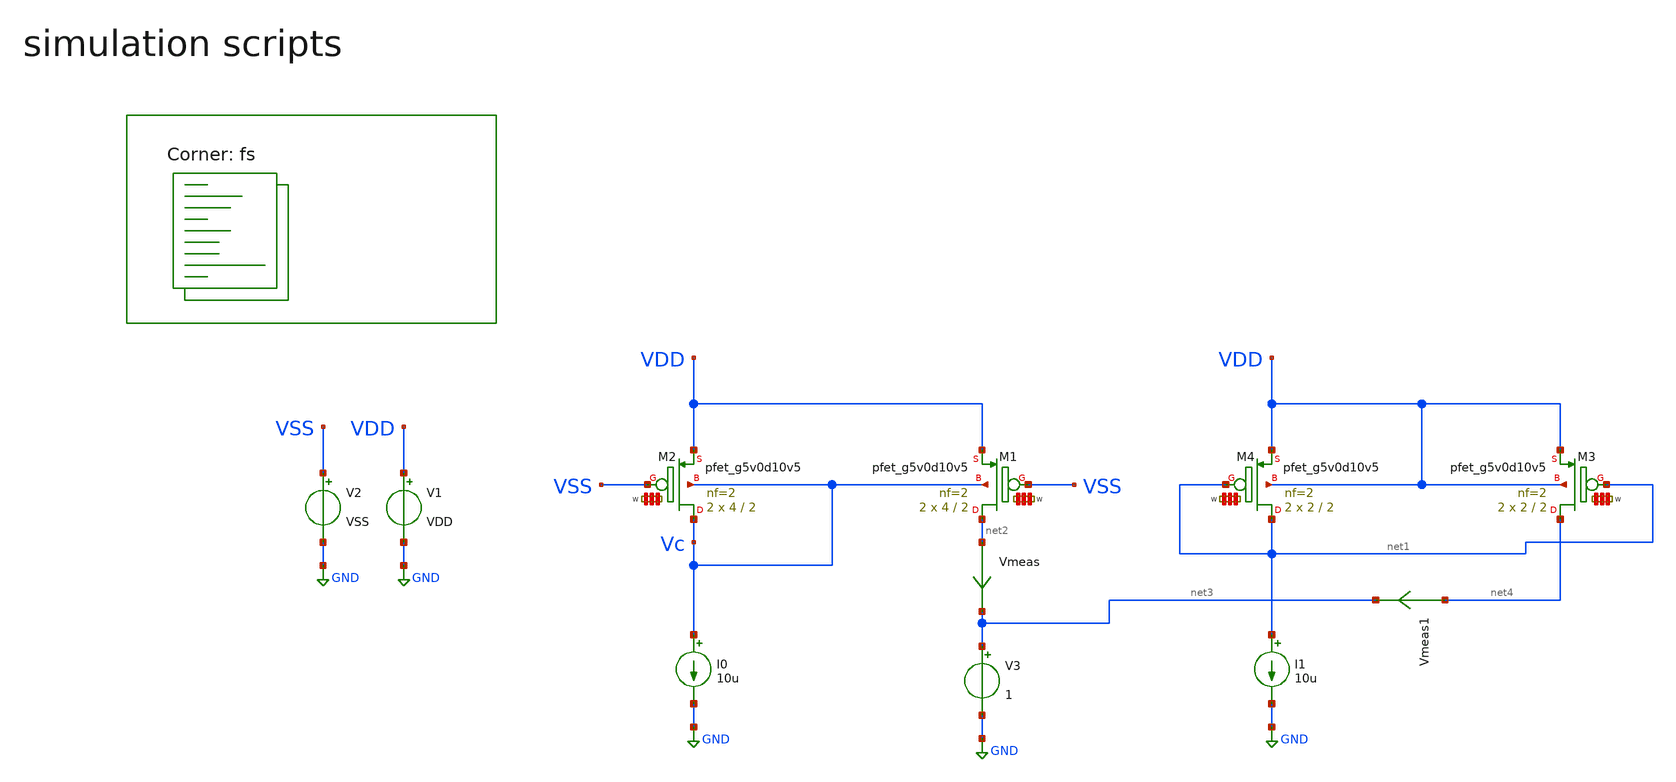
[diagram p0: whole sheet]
** sch_path: Learning/curr_amplifiers/bulk_curr_mir/tb.sch
**.subckt tb
V1 VDD GND VDD
V2 VSS GND VSS
V3 net3 GND 1
I0 Vc GND 10u
XM1 net2 VSS VDD Vc sky130_fd_pr__pfet_g5v0d10v5 L=2 W='4 * 2 ' nf=2 ad='int((2 + 1)/2) * 4 * 0.29' as='int((2 + 2)/2) * 4 * 0.29'
+ pd='2*int((2 + 1)/2) * (4 + 0.29)' ps='2*int((2 + 2)/2) * (4 + 0.29)' nrd='0.29 / 4 / 2 ' nrs='0.29 / 4 / 2 '
+ sa=0 sb=0 sd=0 mult=2 m=2
XM2 Vc VSS VDD Vc sky130_fd_pr__pfet_g5v0d10v5 L=2 W='4 * 2 ' nf=2 ad='int((2 + 1)/2) * 4 * 0.29' as='int((2 + 2)/2) * 4 * 0.29'
+ pd='2*int((2 + 1)/2) * (4 + 0.29)' ps='2*int((2 + 2)/2) * (4 + 0.29)' nrd='0.29 / 4 / 2 ' nrs='0.29 / 4 / 2 '
+ sa=0 sb=0 sd=0 mult=2 m=2
I1 net1 GND 10u
XM3 net4 net1 VDD VDD sky130_fd_pr__pfet_g5v0d10v5 L=2 W='2 * 2 ' nf=2 ad='int((2 + 1)/2) * 2 * 0.29'
+ as='int((2 + 2)/2) * 2 * 0.29' pd='2*int((2 + 1)/2) * (2 + 0.29)' ps='2*int((2 + 2)/2) * (2 + 0.29)'
+ nrd='0.29 / 2 / 2 ' nrs='0.29 / 2 / 2 ' sa=0 sb=0 sd=0 mult=2 m=2
XM4 net1 net1 VDD VDD sky130_fd_pr__pfet_g5v0d10v5 L=2 W='2 * 2 ' nf=2 ad='int((2 + 1)/2) * 2 * 0.29'
+ as='int((2 + 2)/2) * 2 * 0.29' pd='2*int((2 + 1)/2) * (2 + 0.29)' ps='2*int((2 + 2)/2) * (2 + 0.29)'
+ nrd='0.29 / 2 / 2 ' nrs='0.29 / 2 / 2 ' sa=0 sb=0 sd=0 mult=2 m=2
Vmeas net2 net3 0
.save i(vmeas)
Vmeas1 net4 net3 0
.save i(vmeas1)
**** begin user architecture code
.lib $::SKYWATER_MODELS/sky130.lib.spice fs

.Temp 27
.param VDD = 1
.param VSS = 0



.control
save all

dc V3 0 1 0.01
plot i(Vmeas) i(Vmeas1)
plot v(VC)
.endc

**** end user architecture code
**.ends
.GLOBAL GND
.end
